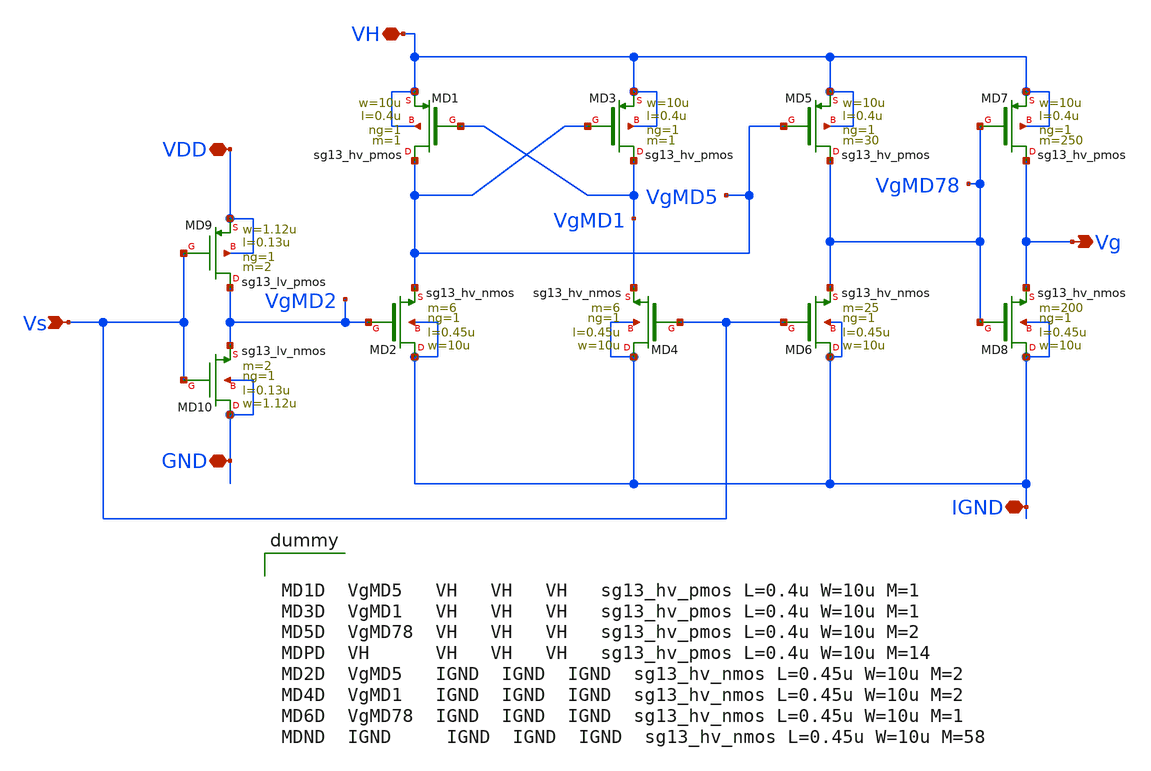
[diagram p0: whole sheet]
** sch_path: ChipUSM_AnalogTrack24/GD/GD_vto2p1.sch
**.subckt GD_vto2p1 VH VDD Vs Vg GND IGND
*.iopin VH
*.iopin VDD
*.ipin Vs
*.opin Vg
*.iopin GND
*.iopin IGND
XMD9 VgMD2 Vs VDD VDD sg13_lv_pmos w=1.12u l=0.13u ng=1 m=2 mm_ok=1
XMD10 GND Vs VgMD2 GND sg13_lv_nmos w=1.12u l=0.13u ng=1 m=2 mm_ok=1
XMD1 VgMD5 VgMD1 VH VH sg13_hv_pmos w=10u l=0.4u ng=1 m=1 mm_ok=1
XMD3 VgMD1 VgMD5 VH VH sg13_hv_pmos w=10u l=0.4u ng=1 m=1 mm_ok=1
XMD5 VgMD78 VgMD5 VH VH sg13_hv_pmos w=10u l=0.4u ng=1 m=30 mm_ok=1
XMD7 Vg VgMD78 VH VH sg13_hv_pmos w=10u l=0.4u ng=1 m=250 mm_ok=1
XMD2 IGND VgMD2 VgMD5 IGND sg13_hv_nmos w=10u l=0.45u ng=1 m=6 mm_ok=1
XMD4 IGND Vs VgMD1 IGND sg13_hv_nmos w=10u l=0.45u ng=1 m=6 mm_ok=1
XMD6 IGND Vs VgMD78 IGND sg13_hv_nmos w=10u l=0.45u ng=1 m=25 mm_ok=1
XMD8 IGND VgMD78 Vg IGND sg13_hv_nmos w=10u l=0.45u ng=1 m=200 mm_ok=1
**** begin user architecture code


MD1D  VgMD5   VH   VH   VH   sg13_hv_pmos L=0.4u W=10u M=1
MD3D  VgMD1   VH   VH   VH   sg13_hv_pmos L=0.4u W=10u M=1
MD5D  VgMD78  VH   VH   VH   sg13_hv_pmos L=0.4u W=10u M=2
MDPD  VH      VH   VH   VH   sg13_hv_pmos L=0.4u W=10u M=14
MD2D  VgMD5   IGND  IGND  IGND  sg13_hv_nmos L=0.45u W=10u M=2
MD4D  VgMD1   IGND  IGND  IGND  sg13_hv_nmos L=0.45u W=10u M=2
MD6D  VgMD78  IGND  IGND  IGND  sg13_hv_nmos L=0.45u W=10u M=1
MDND  IGND     IGND  IGND  IGND  sg13_hv_nmos L=0.45u W=10u M=58


**** end user architecture code
**.ends
.end
